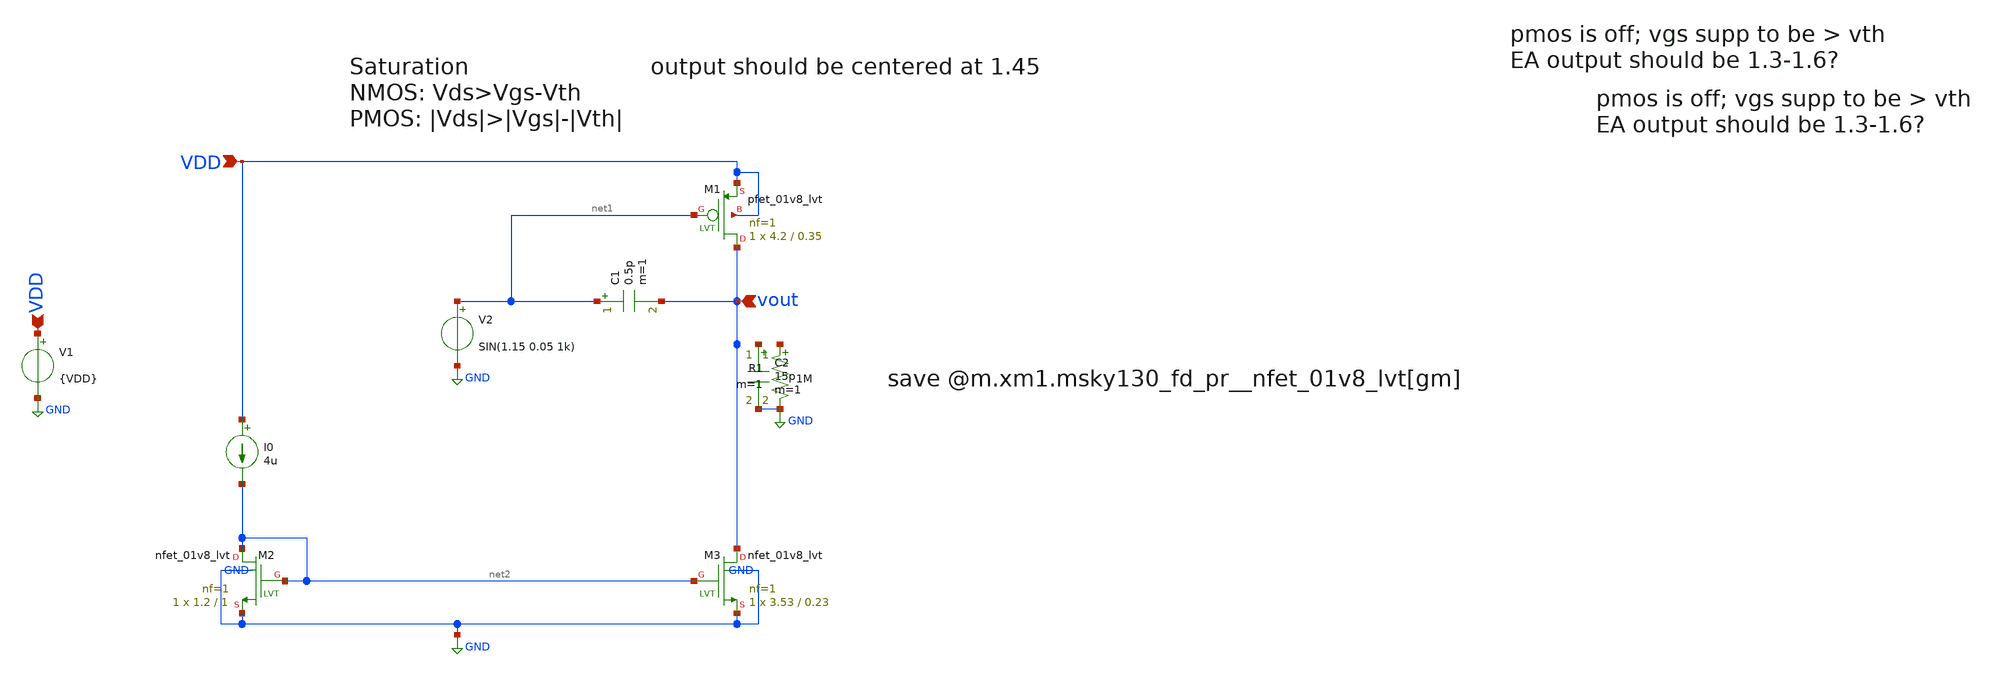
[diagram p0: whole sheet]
** sch_path: xschem/EA/commonsource.sch
**.subckt commonsource VDD VDD vout
*.ipin VDD
*.ipin VDD
*.ipin vout
V1 VDD GND {VDD}
V2 net1 GND SIN(1.15 0.05 1k)
C1 net1 vout 0.5p m=1
XM1 vout net1 VDD VDD sky130_fd_pr__pfet_01v8_lvt L=0.35 W=4.2 nf=1 ad='int((1 + 1)/2) * 4.2 / 1 * 0.29'
+ as='int((1 + 2)/2) * 4.2 / 1 * 0.29' pd='2*int((1 + 1)/2) * (4.2 / 1 + 0.29)' ps='2*int((1 + 2)/2) * (4.2 / 1 + 0.29)'
+ nrd='0.29 / 4.2 ' nrs='0.29 / 4.2 ' sa=0 sb=0 sd=0 mult=1 m=1
I0 VDD net2 4u
XM2 net2 net2 GND GND sky130_fd_pr__nfet_01v8_lvt L=1 W=1.2 nf=1 ad='int((1 + 1)/2) * 1.2 / 1 * 0.29'
+ as='int((1 + 2)/2) * 1.2 / 1 * 0.29' pd='2*int((1 + 1)/2) * (1.2 / 1 + 0.29)' ps='2*int((1 + 2)/2) * (1.2 / 1 + 0.29)'
+ nrd='0.29 / 1.2 ' nrs='0.29 / 1.2 ' sa=0 sb=0 sd=0 mult=1 m=1
XM3 vout net2 GND GND sky130_fd_pr__nfet_01v8_lvt L=0.23 W=3.53 nf=1 ad='int((1 + 1)/2) * 3.53 / 1 * 0.29'
+ as='int((1 + 2)/2) * 3.53 / 1 * 0.29' pd='2*int((1 + 1)/2) * (3.53 / 1 + 0.29)' ps='2*int((1 + 2)/2) * (3.53 / 1 + 0.29)'
+ nrd='0.29 / 3.53 ' nrs='0.29 / 3.53 ' sa=0 sb=0 sd=0 mult=1 m=1
R1 net3 GND 1M m=1
C2 net4 GND 15p m=1
**** begin user architecture code



.lib /usr/local/share/pdk/sky130A/libs.tech/ngspice/sky130.lib.spice tt
.param VDD=1.8 amp=1.2 R=100k L=0.2
.tran 5u 3m
*.dc R 1 1M 10k
.save all

.control
run
print @m.xm1.msky130_fd_pr__pfet_01v8_lvt[vth]
print @m.xm3.msky130_fd_pr__nfet_01v8_lvt[vth]
*plot vout-(v(net2)-@m.xm7.msky130_fd_pr__nfet_01v8[vth])
print 1/@m.xm3.msky130_fd_pr__nfet_01v8_lvt[gds]
print @m.xm1.msky130_fd_pr__pfet_01v8_lvt[gm] * (@m.xm1.msky130_fd_pr__pfet_01v8_lvt[gds] +
+ @m.xm3.msky130_fd_pr__nfet_01v8_lvt[gds])^(-1)
plot vout title vout
*plot db(vout/v(v+))
*plot 180*cph(vout)/pi
set wr_singlescale
set wr_vecnames
*wrdata /foss/designs/2stageCMOSOpAmp/sim_data/GainvsFreq/gain(max).txt db(vout/v(v+))
*wrdata /foss/designs/2stageCMOSOpAmp/sim_data/sample_waves/a1.3m_f1k_gain700.txt vout
*wrdata /foss/designs/2stageCMOSOpAmp/sim_data/SR/SR.txt vout

.endc


**** end user architecture code
**.ends
.GLOBAL GND
.end
